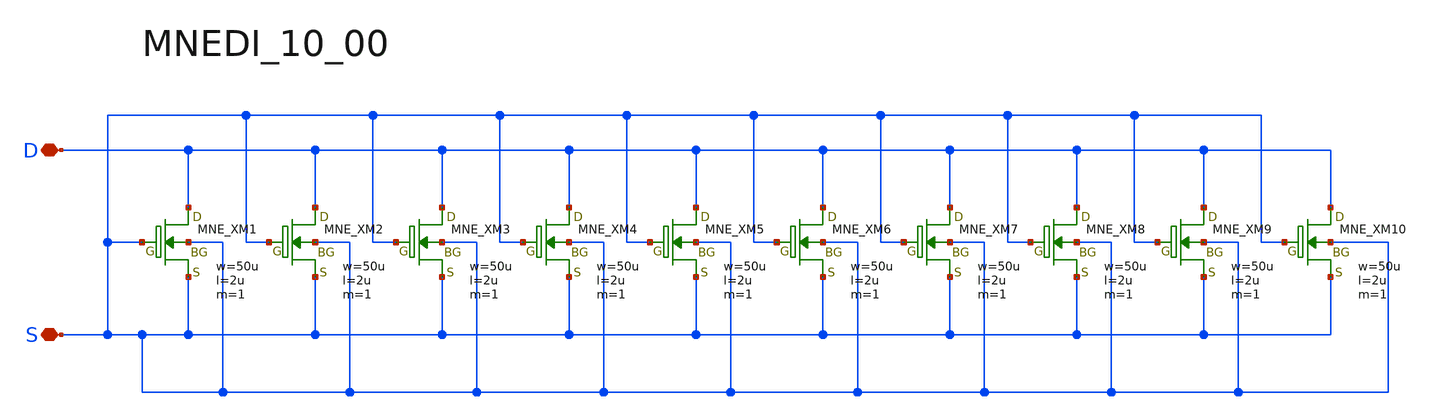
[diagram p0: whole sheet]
** sch_path: libs.tech/xschem/TR-1um_2_ESD/MNEDI_10_00.sch
**.subckt MNEDI_10_00 D S
*.iopin D
*.iopin S
XXM1 D S S S MNE w=50u l=2u as=0 ad=0 ps=0 pd=0 nrd=0 nrs=0 m=1
XXM2 D S S S MNE w=50u l=2u as=0 ad=0 ps=0 pd=0 nrd=0 nrs=0 m=1
XXM3 D S S S MNE w=50u l=2u as=0 ad=0 ps=0 pd=0 nrd=0 nrs=0 m=1
XXM4 D S S S MNE w=50u l=2u as=0 ad=0 ps=0 pd=0 nrd=0 nrs=0 m=1
XXM5 D S S S MNE w=50u l=2u as=0 ad=0 ps=0 pd=0 nrd=0 nrs=0 m=1
XXM6 D S S S MNE w=50u l=2u as=0 ad=0 ps=0 pd=0 nrd=0 nrs=0 m=1
XXM7 D S S S MNE w=50u l=2u as=0 ad=0 ps=0 pd=0 nrd=0 nrs=0 m=1
XXM8 D S S S MNE w=50u l=2u as=0 ad=0 ps=0 pd=0 nrd=0 nrs=0 m=1
XXM9 D S S S MNE w=50u l=2u as=0 ad=0 ps=0 pd=0 nrd=0 nrs=0 m=1
XXM10 D S S S MNE w=50u l=2u as=0 ad=0 ps=0 pd=0 nrd=0 nrs=0 m=1
**.ends
.end
